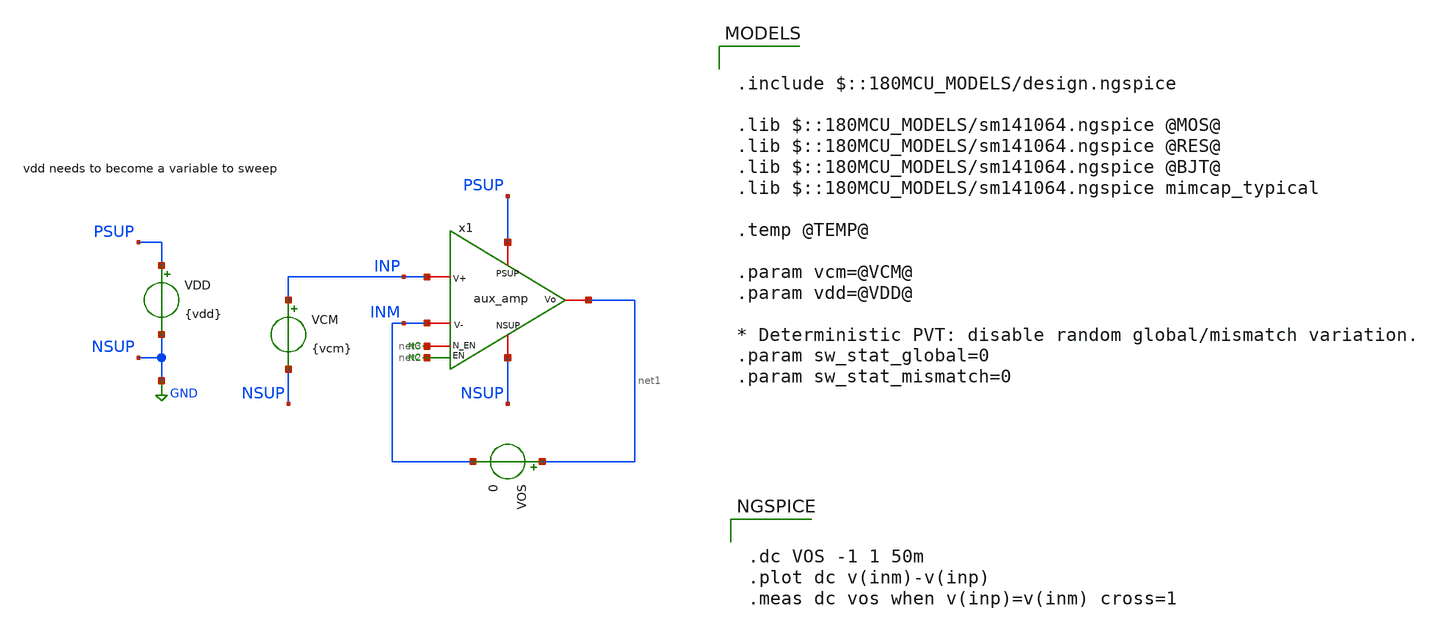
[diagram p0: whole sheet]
** sch_path: xschem/blocks/aux_amp/tb_aux_amp_offset.sch
**.subckt tb_aux_amp_offset
VDD PSUP NSUP {vdd}
VCM INP NSUP {vcm}
* noconn #net2
* noconn #net3
x1 PSUP net1 INP INM net3 NSUP net2 aux_amp
VOS net1 INM 0
**** begin user architecture code


.dc VOS -1 1 50m
.plot dc v(inm)-v(inp)
.meas dc vos when v(inp)=v(inm) cross=1




.include $::180MCU_MODELS/design.ngspice

.lib $::180MCU_MODELS/sm141064.ngspice @MOS@
.lib $::180MCU_MODELS/sm141064.ngspice @RES@
.lib $::180MCU_MODELS/sm141064.ngspice @BJT@
.lib $::180MCU_MODELS/sm141064.ngspice mimcap_typical

.temp @TEMP@

.param vcm=@VCM@
.param vdd=@VDD@

* Deterministic PVT: disable random global/mismatch variation.
.param sw_stat_global=0
.param sw_stat_mismatch=0



**** end user architecture code
**.ends

* expanding   symbol:  blocks/aux_amp/aux_amp.sym # of pins=7
** sym_path: xschem/lib/aux_amp.sym
** sch_path: xschem/lib/aux_amp.sch
.subckt aux_amp PSUP Vo V+ V- N_EN NSUP EN
*.ipin PSUP
*.ipin NSUP
*.ipin N_EN
*.ipin EN
*.ipin V+
*.ipin V-
*.opin Vo
XM1 Vo V- net2 net2 nfet_06v0 L=1.80u W=0.80u nf=1 ad='int((nf+1)/2) * W/nf * 0.18u' as='int((nf+2)/2) * W/nf * 0.18u'
+ pd='2*int((nf+1)/2) * (W/nf + 0.18u)' ps='2*int((nf+2)/2) * (W/nf + 0.18u)' nrd='0.18u / W' nrs='0.18u / W'
+ sa=0 sb=0 sd=0 m=1
XM2 net1 V+ net2 net2 nfet_06v0 L=1.80u W=0.80u nf=1 ad='int((nf+1)/2) * W/nf * 0.18u' as='int((nf+2)/2) * W/nf * 0.18u'
+ pd='2*int((nf+1)/2) * (W/nf + 0.18u)' ps='2*int((nf+2)/2) * (W/nf + 0.18u)' nrd='0.18u / W' nrs='0.18u / W'
+ sa=0 sb=0 sd=0 m=1
XM5 net1 net1 PSUP PSUP pfet_06v0 L=0.55u W=0.30u nf=1 ad='int((nf+1)/2) * W/nf * 0.18u' as='int((nf+2)/2) * W/nf * 0.18u'
+ pd='2*int((nf+1)/2) * (W/nf + 0.18u)' ps='2*int((nf+2)/2) * (W/nf + 0.18u)' nrd='0.18u / W' nrs='0.18u / W'
+ sa=0 sb=0 sd=0 m=1
XM6 Vo net1 PSUP PSUP pfet_06v0 L=0.55u W=0.30u nf=1 ad='int((nf+1)/2) * W/nf * 0.18u' as='int((nf+2)/2) * W/nf * 0.18u'
+ pd='2*int((nf+1)/2) * (W/nf + 0.18u)' ps='2*int((nf+2)/2) * (W/nf + 0.18u)' nrd='0.18u / W' nrs='0.18u / W'
+ sa=0 sb=0 sd=0 m=1
I0 net2 NSUP 5u
* noconn N_EN
* noconn EN
.ends

.GLOBAL GND
.end
